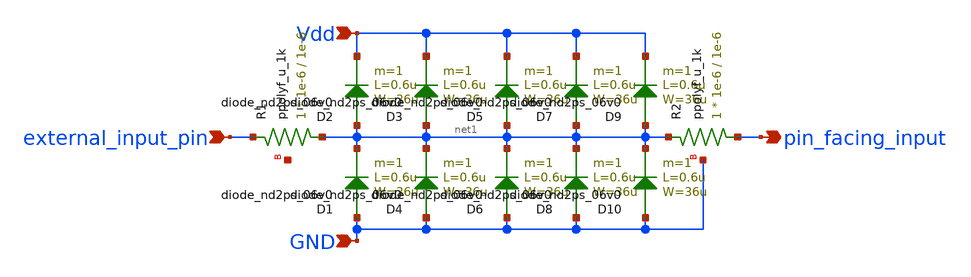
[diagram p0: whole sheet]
** sch_path: MRTMOS_final_chip/MG_ESD_protection.sch
**.subckt MG_ESD_protection external_input_pin Vdd GND pin_facing_input
*.ipin external_input_pin
*.ipin Vdd
*.ipin GND
*.opin pin_facing_input
D2 net1 Vdd diode_nd2ps_06v0 area='36u * 0.6u ' pj='2*36u + 2*0.6u ' m=1
D1 GND net1 diode_nd2ps_06v0 area='36u * 0.6u ' pj='2*36u + 2*0.6u ' m=1
XR1 net1 external_input_pin net2 ppolyf_u_1k r_width=1e-6 r_length=1e-6 m=1
D3 net1 Vdd diode_nd2ps_06v0 area='36u * 0.6u ' pj='2*36u + 2*0.6u ' m=1
D4 GND net1 diode_nd2ps_06v0 area='36u * 0.6u ' pj='2*36u + 2*0.6u ' m=1
D5 net1 Vdd diode_nd2ps_06v0 area='36u * 0.6u ' pj='2*36u + 2*0.6u ' m=1
D6 GND net1 diode_nd2ps_06v0 area='36u * 0.6u ' pj='2*36u + 2*0.6u ' m=1
D7 net1 Vdd diode_nd2ps_06v0 area='36u * 0.6u ' pj='2*36u + 2*0.6u ' m=1
D8 GND net1 diode_nd2ps_06v0 area='36u * 0.6u ' pj='2*36u + 2*0.6u ' m=1
D9 net1 Vdd diode_nd2ps_06v0 area='36u * 0.6u ' pj='2*36u + 2*0.6u ' m=1
D10 GND net1 diode_nd2ps_06v0 area='36u * 0.6u ' pj='2*36u + 2*0.6u ' m=1
XR2 pin_facing_input net1 GND ppolyf_u_1k r_width=1e-6 r_length=1e-6 m=1
**.ends
.end
